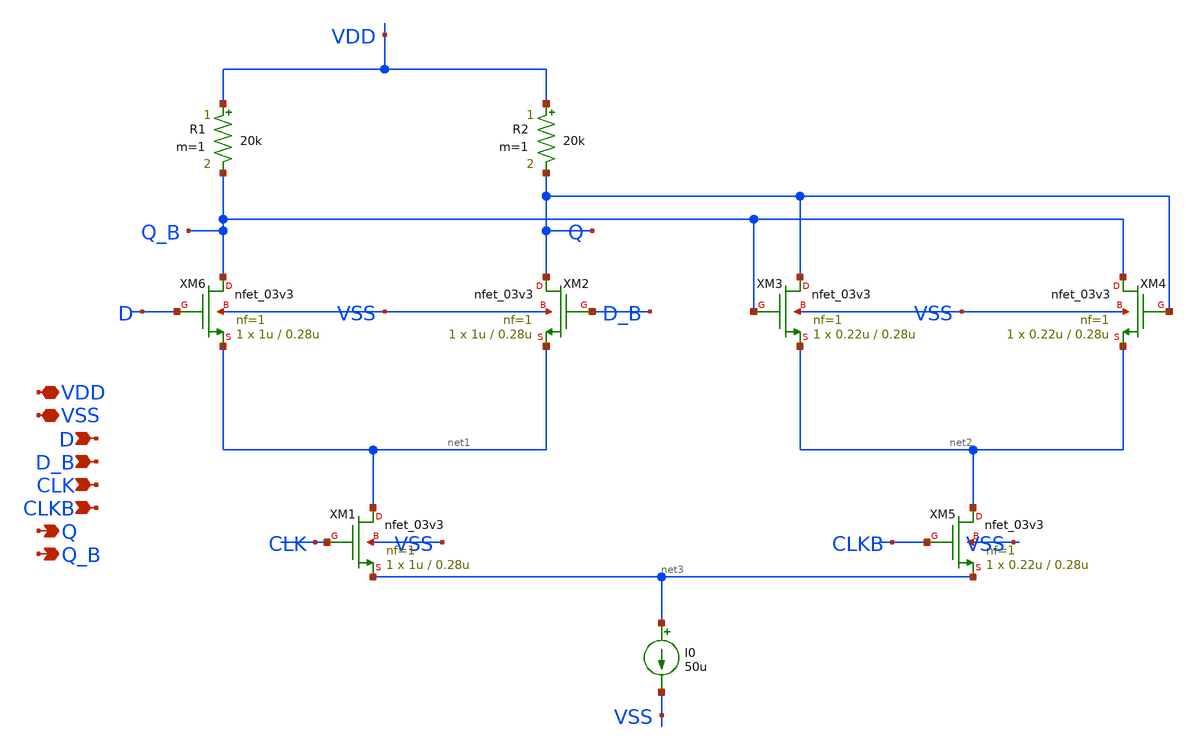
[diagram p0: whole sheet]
** sch_path: DAC_PAKISTAN_01/Pakistan1_Xschem/CMLL.sch
**.subckt CMLL VDD VSS D D_B CLK CLKB Q Q_B
*.iopin VDD
*.iopin VSS
*.ipin D
*.ipin D_B
*.ipin CLK
*.ipin CLKB
*.opin Q
*.opin Q_B
XM2 Q D_B net1 VSS nfet_03v3 L=0.28u W=1u nf=1 ad='int((nf+1)/2) * W/nf * 0.18u' as='int((nf+2)/2) * W/nf * 0.18u'
+ pd='2*int((nf+1)/2) * (W/nf + 0.18u)' ps='2*int((nf+2)/2) * (W/nf + 0.18u)' nrd='0.18u / W' nrs='0.18u / W'
+ sa=0 sb=0 sd=0 m=1
XM3 Q Q_B net2 VSS nfet_03v3 L=0.28u W=0.22u nf=1 ad='int((nf+1)/2) * W/nf * 0.18u' as='int((nf+2)/2) * W/nf * 0.18u'
+ pd='2*int((nf+1)/2) * (W/nf + 0.18u)' ps='2*int((nf+2)/2) * (W/nf + 0.18u)' nrd='0.18u / W' nrs='0.18u / W'
+ sa=0 sb=0 sd=0 m=1
XM4 Q_B Q net2 VSS nfet_03v3 L=0.28u W=0.22u nf=1 ad='int((nf+1)/2) * W/nf * 0.18u' as='int((nf+2)/2) * W/nf * 0.18u'
+ pd='2*int((nf+1)/2) * (W/nf + 0.18u)' ps='2*int((nf+2)/2) * (W/nf + 0.18u)' nrd='0.18u / W' nrs='0.18u / W'
+ sa=0 sb=0 sd=0 m=1
XM5 net2 CLKB net3 VSS nfet_03v3 L=0.28u W=0.22u nf=1 ad='int((nf+1)/2) * W/nf * 0.18u' as='int((nf+2)/2) * W/nf * 0.18u'
+ pd='2*int((nf+1)/2) * (W/nf + 0.18u)' ps='2*int((nf+2)/2) * (W/nf + 0.18u)' nrd='0.18u / W' nrs='0.18u / W'
+ sa=0 sb=0 sd=0 m=1
XM6 Q_B D net1 VSS nfet_03v3 L=0.28u W=1u nf=1 ad='int((nf+1)/2) * W/nf * 0.18u' as='int((nf+2)/2) * W/nf * 0.18u'
+ pd='2*int((nf+1)/2) * (W/nf + 0.18u)' ps='2*int((nf+2)/2) * (W/nf + 0.18u)' nrd='0.18u / W' nrs='0.18u / W'
+ sa=0 sb=0 sd=0 m=1
R1 VDD Q_B 20k m=1
R2 VDD Q 20k m=1
I0 net3 VSS 50u
XM1 net1 CLK net3 VSS nfet_03v3 L=0.28u W=1u nf=1 ad='int((nf+1)/2) * W/nf * 0.18u' as='int((nf+2)/2) * W/nf * 0.18u'
+ pd='2*int((nf+1)/2) * (W/nf + 0.18u)' ps='2*int((nf+2)/2) * (W/nf + 0.18u)' nrd='0.18u / W' nrs='0.18u / W'
+ sa=0 sb=0 sd=0 m=1
**.ends
.end
